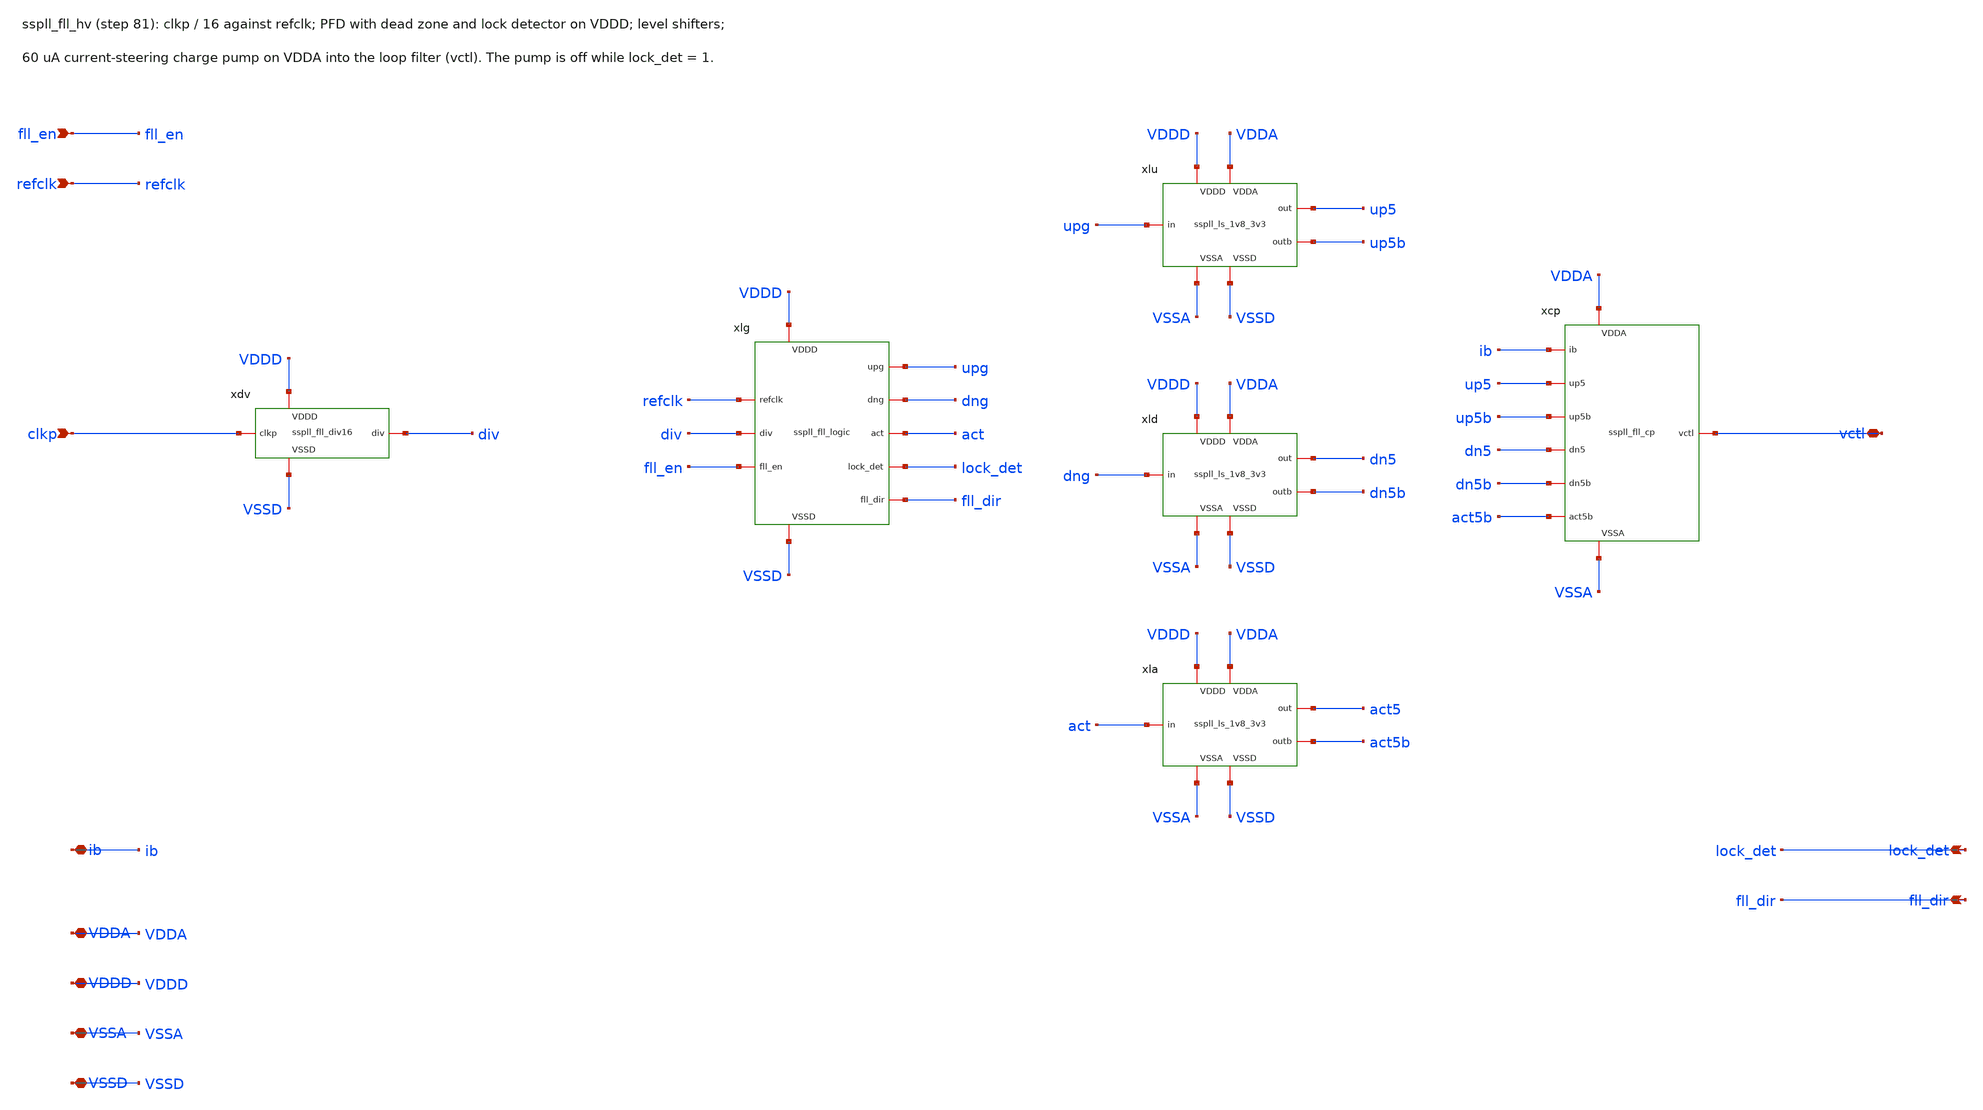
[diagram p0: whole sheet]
** sch_path: xschem/fll_hv/sspll_fll_hv.sch
**.subckt sspll_fll_hv clkp refclk fll_en vctl ib lock_det fll_dir VDDA VDDD VSSA VSSD
*.ipin clkp
*.ipin refclk
*.ipin fll_en
*.iopin vctl
*.iopin ib
*.opin lock_det
*.opin fll_dir
*.iopin VDDA
*.iopin VDDD
*.iopin VSSA
*.iopin VSSD
xdv clkp div VDDD VSSD sspll_fll_div16
xlg refclk div fll_en upg dng act lock_det fll_dir VDDD VSSD sspll_fll_logic
xlu upg up5 up5b VDDD VDDA VSSA VSSD sspll_ls_1v8_3v3
xld dng dn5 dn5b VDDD VDDA VSSA VSSD sspll_ls_1v8_3v3
xla act act5 act5b VDDD VDDA VSSA VSSD sspll_ls_1v8_3v3
xcp ib up5 up5b dn5 dn5b act5b vctl VDDA VSSA sspll_fll_cp
**.ends
.end
